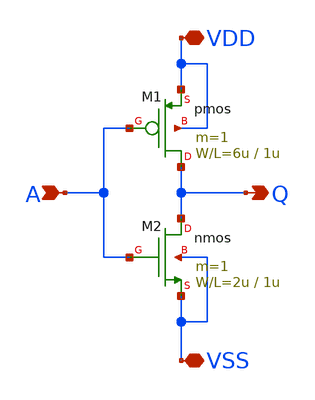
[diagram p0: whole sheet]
** sch_path: member_project/sanken/yamazaki/inverter_OR1/inverter_OR1.sch
**.subckt inverter_OR1 VDD VSS A Q
*.iopin VDD
*.iopin VSS
*.ipin A
*.opin Q
M1 Q A VDD VDD pmos L=1u W=6u m=1
M2 Q A VSS VSS nmos L=1u W=2u m=1
**.ends
.end
